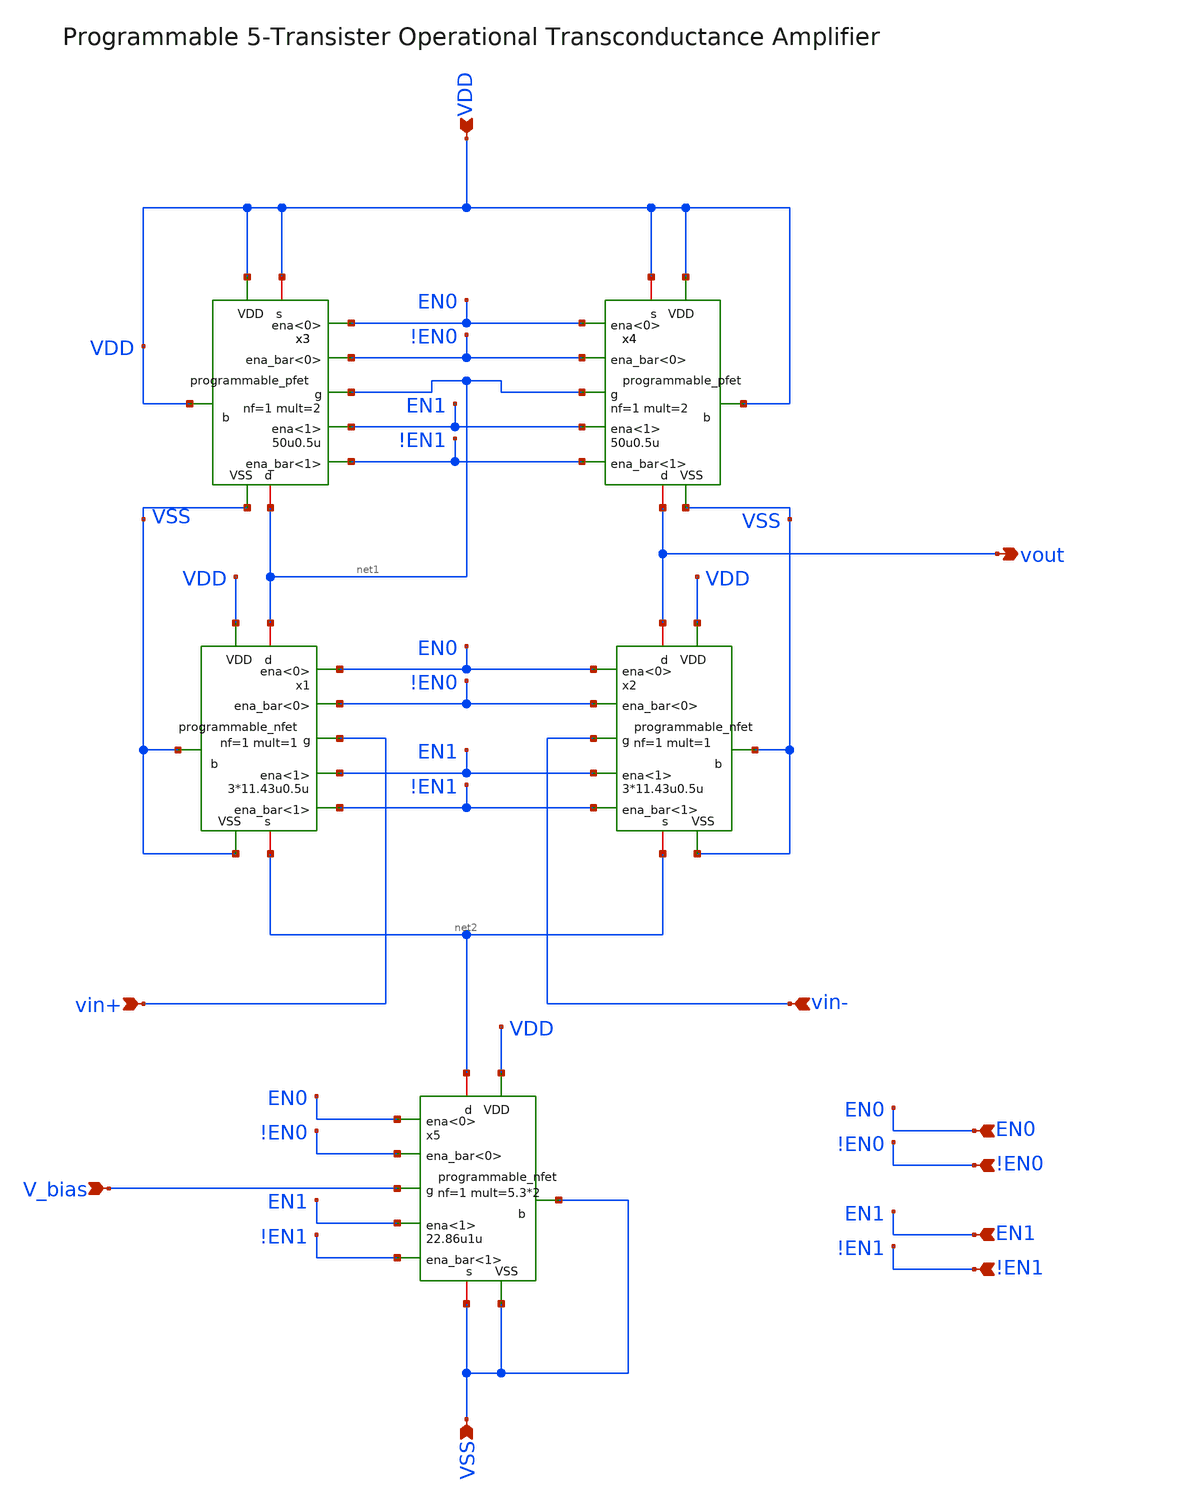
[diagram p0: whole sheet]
** sch_path: designs/libs/core_amps/ota_5t/prgram_schem/programmable_5tOTA.sch
**.subckt programmable_5tOTA VDD vout vin+ vin- V_bias VSS EN0 !EN0 EN1 !EN1
*.ipin VDD
*.opin vout
*.ipin vin+
*.ipin vin-
*.ipin V_bias
*.ipin VSS
*.ipin EN0
*.ipin !EN0
*.ipin EN1
*.ipin !EN1
x1 net1 VSS vin+ net2 !EN0 VDD !EN1 EN0 EN1 VSS programmable_nfet width=3*11.43u length=0.5u nf=1
+ mult=1
x2 vout VSS vin- net2 !EN0 VDD !EN1 EN0 EN1 VSS programmable_nfet width=3*11.43u length=0.5u nf=1
+ mult=1
x4 vout VDD net1 VDD !EN0 VDD !EN1 EN0 EN1 VSS programmable_pfet width=50u length=0.5u nf=1 mult=2
x3 net1 VDD net1 VDD !EN0 VDD !EN1 EN0 EN1 VSS programmable_pfet width=50u length=0.5u nf=1 mult=2
x5 net2 VSS V_bias VSS !EN0 VDD !EN1 EN0 EN1 VSS programmable_nfet width=22.86u length=1u nf=1
+ mult=5.3*2
**.ends

* expanding   symbol:  libs/core_digital/schem/programmable_nfet.sym # of pins=10
** sym_path: designs/libs/core_digital/schem/programmable_nfet.sym
** sch_path: designs/libs/core_digital/schem/programmable_nfet.sch
.subckt programmable_nfet d b g s ena_bar<0> VDD ena_bar<1> ena<0> ena<1> VSS  width=0.22u
+ length=0.28u nf=1 mult=1
*.ipin VSS
*.ipin VDD
*.ipin g
*.ipin ena_bar<1>
*.ipin ena_bar<0>
*.ipin ena<1>
*.ipin ena<0>
*.iopin d
*.iopin s
*.ipin b
XM1 d net2 s b nfet_03v3 L={length} W={width} nf={nf} ad='int((nf+1)/2) * W/nf * 0.18u' as='int((nf+2)/2) * W/nf * 0.18u'
+ pd='2*int((nf+1)/2) * (W/nf + 0.18u)' ps='2*int((nf+2)/2) * (W/nf + 0.18u)' nrd='0.18u / W' nrs='0.18u / W'
+ sa=0 sb=0 sd=0 m={mult}
XM3 d net1 s b nfet_03v3 L={length} W={2*width} nf={2*nf} ad='int((nf+1)/2) * W/nf * 0.18u' as='int((nf+2)/2) * W/nf * 0.18u'
+ pd='2*int((nf+1)/2) * (W/nf + 0.18u)' ps='2*int((nf+2)/2) * (W/nf + 0.18u)' nrd='0.18u / W' nrs='0.18u / W'
+ sa=0 sb=0 sd=0 m={mult}
XM2 net1 ena_bar<1> VSS VSS nfet_03v3 L=0.28u W=0.22u nf=1 ad='int((nf+1)/2) * W/nf * 0.18u' as='int((nf+2)/2) * W/nf * 0.18u'
+ pd='2*int((nf+1)/2) * (W/nf + 0.18u)' ps='2*int((nf+2)/2) * (W/nf + 0.18u)' nrd='0.18u / W' nrs='0.18u / W'
+ sa=0 sb=0 sd=0 m=1
XM4 net2 ena_bar<0> VSS VSS nfet_03v3 L=0.28u W=0.22u nf=1 ad='int((nf+1)/2) * W/nf * 0.18u' as='int((nf+2)/2) * W/nf * 0.18u'
+ pd='2*int((nf+1)/2) * (W/nf + 0.18u)' ps='2*int((nf+2)/2) * (W/nf + 0.18u)' nrd='0.18u / W' nrs='0.18u / W'
+ sa=0 sb=0 sd=0 m=1
x1 ena_bar<0> VDD net2 g VSS ena<0> transmission_gate
x2 ena_bar<1> VDD net1 g VSS ena<1> transmission_gate
.ends


* expanding   symbol:  libs/core_digital/schem/programmable_pfet.sym # of pins=10
** sym_path: designs/libs/core_digital/schem/programmable_pfet.sym
** sch_path: designs/libs/core_digital/schem/programmable_pfet.sch
.subckt programmable_pfet d b g s ena_bar<0> VDD ena_bar<1> ena<0> ena<1> VSS  width=0.22u
+ length=0.28u nf=1 mult=1
*.ipin VSS
*.ipin VDD
*.ipin g
*.ipin ena_bar<1>
*.ipin ena_bar<0>
*.ipin ena<0>
*.iopin s
*.iopin d
*.ipin b
*.ipin ena<1>
XM1 d net2 s b pfet_03v3 L={length} W={width} nf={nf} ad='int((nf+1)/2) * W/nf * 0.18u' as='int((nf+2)/2) * W/nf * 0.18u'
+ pd='2*int((nf+1)/2) * (W/nf + 0.18u)' ps='2*int((nf+2)/2) * (W/nf + 0.18u)' nrd='0.18u / W' nrs='0.18u / W'
+ sa=0 sb=0 sd=0 m={mult}
XM3 d net1 s b pfet_03v3 L={length} W={2*width} nf={2*nf} ad='int((nf+1)/2) * W/nf * 0.18u' as='int((nf+2)/2) * W/nf * 0.18u'
+ pd='2*int((nf+1)/2) * (W/nf + 0.18u)' ps='2*int((nf+2)/2) * (W/nf + 0.18u)' nrd='0.18u / W' nrs='0.18u / W'
+ sa=0 sb=0 sd=0 m={mult}
XM2 net1 ena<1> VDD VDD pfet_03v3 L=0.28u W=0.22u nf=1 ad='int((nf+1)/2) * W/nf * 0.18u' as='int((nf+2)/2) * W/nf * 0.18u'
+ pd='2*int((nf+1)/2) * (W/nf + 0.18u)' ps='2*int((nf+2)/2) * (W/nf + 0.18u)' nrd='0.18u / W' nrs='0.18u / W'
+ sa=0 sb=0 sd=0 m=1
XM4 net2 ena<0> VDD VDD pfet_03v3 L=0.28u W=0.22u nf=1 ad='int((nf+1)/2) * W/nf * 0.18u' as='int((nf+2)/2) * W/nf * 0.18u'
+ pd='2*int((nf+1)/2) * (W/nf + 0.18u)' ps='2*int((nf+2)/2) * (W/nf + 0.18u)' nrd='0.18u / W' nrs='0.18u / W'
+ sa=0 sb=0 sd=0 m=1
x1 ena_bar<0> VDD net2 g VSS ena<0> transmission_gate
x2 ena_bar<1> VDD net1 g VSS ena<1> transmission_gate
.ends


* expanding   symbol:  libs/core_digital/schem/transmission_gate.sym # of pins=6
** sym_path: designs/libs/core_digital/schem/transmission_gate.sym
** sch_path: designs/libs/core_digital/schem/transmission_gate.sch
.subckt transmission_gate ena_bar VDD out in VSS ena
*.ipin in
*.ipin ena_bar
*.ipin ena
*.ipin VSS
*.ipin VDD
*.opin out
XM1 in ena_bar out VDD pfet_03v3 L=0.28u W=0.22u nf=1 ad='int((nf+1)/2) * W/nf * 0.18u' as='int((nf+2)/2) * W/nf * 0.18u'
+ pd='2*int((nf+1)/2) * (W/nf + 0.18u)' ps='2*int((nf+2)/2) * (W/nf + 0.18u)' nrd='0.18u / W' nrs='0.18u / W'
+ sa=0 sb=0 sd=0 m=1
XM2 in ena out VSS nfet_03v3 L=0.28u W=0.22u nf=1 ad='int((nf+1)/2) * W/nf * 0.18u' as='int((nf+2)/2) * W/nf * 0.18u'
+ pd='2*int((nf+1)/2) * (W/nf + 0.18u)' ps='2*int((nf+2)/2) * (W/nf + 0.18u)' nrd='0.18u / W' nrs='0.18u / W'
+ sa=0 sb=0 sd=0 m=1
.ends

.end
